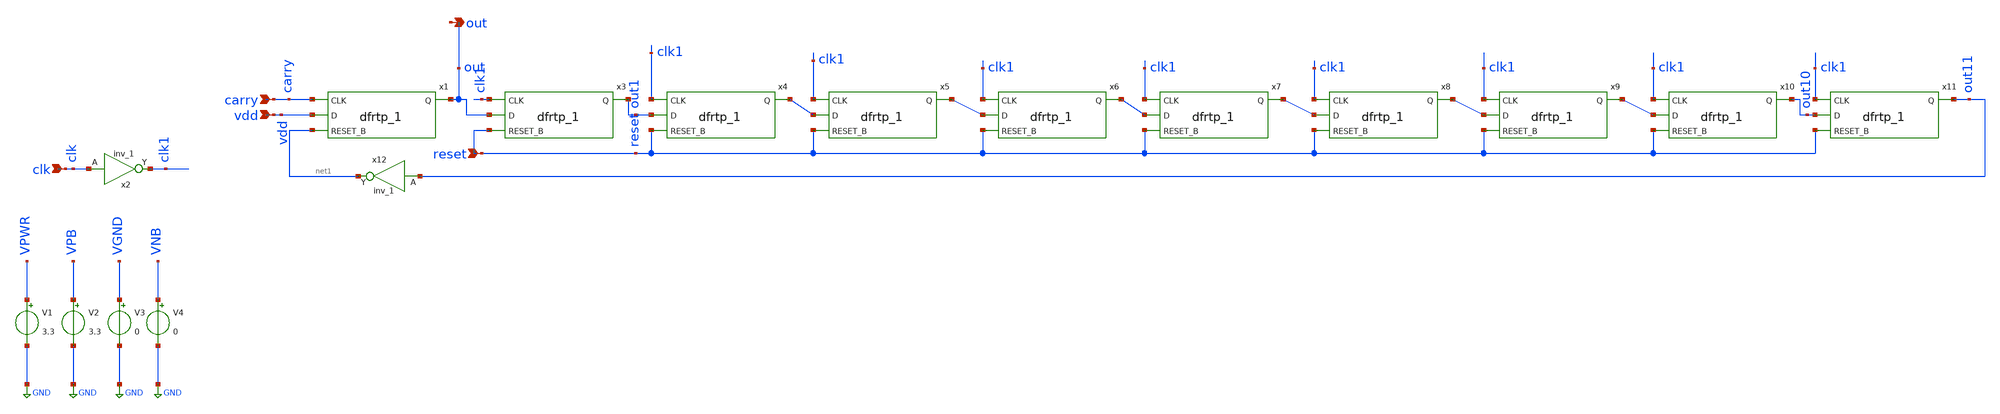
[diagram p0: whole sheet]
** sch_path: xschem/FDC/delay1.sch
**.subckt delay1 clk carry out reset vdd
*.ipin clk
*.ipin carry
*.opin out
*.ipin reset
*.ipin vdd
x1 carry vdd net1 VGND VNB VPB VPWR out sky130_fd_sc_hvl__dfrtp_1
x2 clk VGND VNB VPB VPWR clk1 sky130_fd_sc_hvl__inv_1
x3 clk1 out reset VGND VNB VPB VPWR out1 sky130_fd_sc_hvl__dfrtp_1
x4 clk1 out1 reset VGND VNB VPB VPWR net2 sky130_fd_sc_hvl__dfrtp_1
x5 clk1 net2 reset VGND VNB VPB VPWR net3 sky130_fd_sc_hvl__dfrtp_1
x6 clk1 net3 reset VGND VNB VPB VPWR net4 sky130_fd_sc_hvl__dfrtp_1
x7 clk1 net4 reset VGND VNB VPB VPWR net5 sky130_fd_sc_hvl__dfrtp_1
x8 clk1 net5 reset VGND VNB VPB VPWR net6 sky130_fd_sc_hvl__dfrtp_1
x9 clk1 net6 reset VGND VNB VPB VPWR net7 sky130_fd_sc_hvl__dfrtp_1
x10 clk1 net7 reset VGND VNB VPB VPWR out10 sky130_fd_sc_hvl__dfrtp_1
x11 clk1 out10 reset VGND VNB VPB VPWR out11 sky130_fd_sc_hvl__dfrtp_1
V1 VPWR GND 3.3
V2 VPB GND 3.3
V3 VGND GND 0
V4 VNB GND 0
x12 out11 VGND VNB VPB VPWR net1 sky130_fd_sc_hvl__inv_1
**** begin user architecture code

.lib ~/open_pdks/sky130/sky130A/libs.tech/ngspice/sky130.lib.spice tt
.include /home/vinodhini/open_pdks/sky130/sky130A/libs.ref/sky130_fd_sc_hvl/spice/sky130_fd_sc_hvl.spice

*.MODEL swmod SW(VT=0.0 VH=0.01 RON=1 ROFF=10000000000)
.param mc_mm_switch=0
.param mc_pr_switch=0


.tran 2.5u 1m
.options gmin=1E-11
.save carry reset clk clk1 out out1 out10 out11

**** end user architecture code
**.ends
.GLOBAL GND
.end
